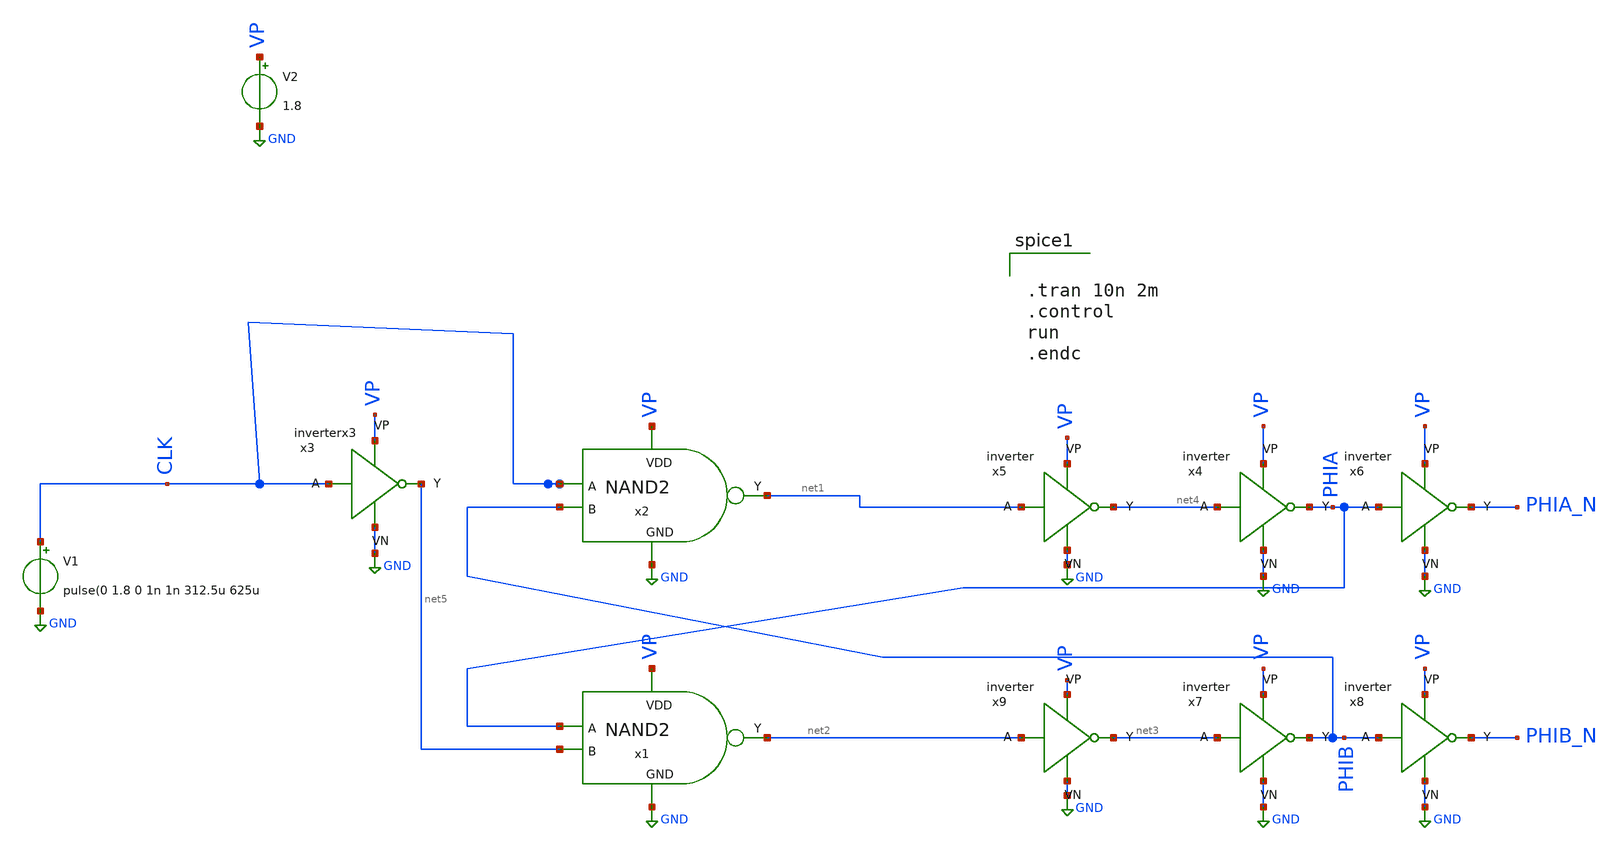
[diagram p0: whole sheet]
** sch_path: ADC/16bit_C2C/MagicAndSpice/EE431_FinalProj/clock_test.sch
**.subckt clock_test
V1 CLK GND pulse(0 1.8 0 1n 1n 312.5u 625u
V2 VP GND 1.8
x5 net1 net4 VP GND inverter
x9 net2 net3 VP GND inverter
x1 VP net2 PHIA net5 GND NAND2
x2 VP net1 CLK PHIB GND NAND2
x3 CLK net5 VP GND inverterx3
x4 net4 PHIA VP GND inverter
x6 PHIA PHIA_N VP GND inverter
x7 net3 PHIB VP GND inverter
x8 PHIB PHIB_N VP GND inverter
**** begin user architecture code
 .lib $::SKYWATER_MODELS/sky130.lib.spice tt


.tran 10n 2m
.control
run
.endc

**** end user architecture code
**.ends
.GLOBAL GND
.end
